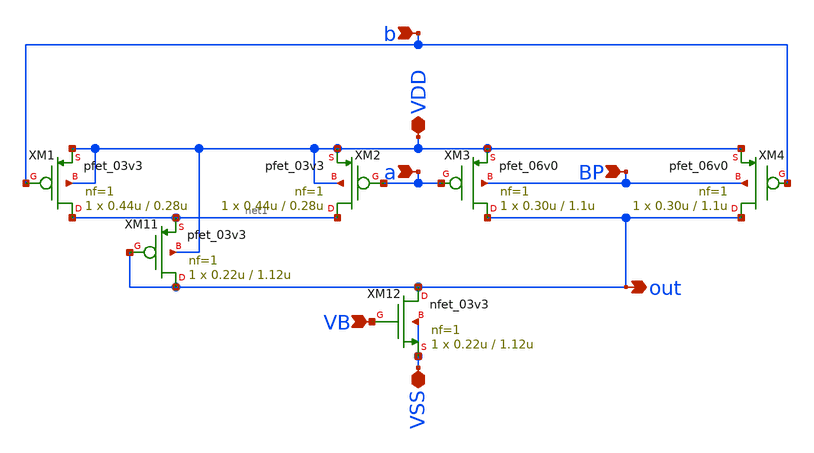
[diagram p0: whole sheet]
** sch_path: xschem_sn2/NMIN.sch
**.subckt NMIN BP VDD out a b VSS VB
*.ipin BP
*.iopin VDD
*.opin out
*.ipin a
*.ipin b
*.iopin VSS
*.ipin VB
XM1 net1 b VDD VDD pfet_03v3 L=0.28u W=0.44u nf=1 ad='int((nf+1)/2) * W/nf * 0.18u' as='int((nf+2)/2) * W/nf * 0.18u'
+ pd='2*int((nf+1)/2) * (W/nf + 0.18u)' ps='2*int((nf+2)/2) * (W/nf + 0.18u)' nrd='0.18u / W' nrs='0.18u / W'
+ sa=0 sb=0 sd=0 m=1 par=1
XM2 net1 a VDD VDD pfet_03v3 L=0.28u W=0.44u nf=1 ad='int((nf+1)/2) * W/nf * 0.18u' as='int((nf+2)/2) * W/nf * 0.18u'
+ pd='2*int((nf+1)/2) * (W/nf + 0.18u)' ps='2*int((nf+2)/2) * (W/nf + 0.18u)' nrd='0.18u / W' nrs='0.18u / W'
+ sa=0 sb=0 sd=0 m=1 par=1
XM3 out a VDD BP pfet_06v0 L=1.1u W=0.30u nf=1 ad='int((nf+1)/2) * W/nf * 0.18u' as='int((nf+2)/2) * W/nf * 0.18u'
+ pd='2*int((nf+1)/2) * (W/nf + 0.18u)' ps='2*int((nf+2)/2) * (W/nf + 0.18u)' nrd='0.18u / W' nrs='0.18u / W'
+ sa=0 sb=0 sd=0 m=1
XM4 out b VDD BP pfet_06v0 L=1.1u W=0.30u nf=1 ad='int((nf+1)/2) * W/nf * 0.18u' as='int((nf+2)/2) * W/nf * 0.18u'
+ pd='2*int((nf+1)/2) * (W/nf + 0.18u)' ps='2*int((nf+2)/2) * (W/nf + 0.18u)' nrd='0.18u / W' nrs='0.18u / W'
+ sa=0 sb=0 sd=0 m=1
XM11 out out net1 VDD pfet_03v3 L=1.12u W=0.22u nf=1 ad='int((nf+1)/2) * W/nf * 0.18u' as='int((nf+2)/2) * W/nf * 0.18u'
+ pd='2*int((nf+1)/2) * (W/nf + 0.18u)' ps='2*int((nf+2)/2) * (W/nf + 0.18u)' nrd='0.18u / W' nrs='0.18u / W'
+ sa=0 sb=0 sd=0 m=1 par=1
XM12 out VB VSS VSS nfet_03v3 L=1.12u W=0.22u nf=1 ad='int((nf+1)/2) * W/nf * 0.18u' as='int((nf+2)/2) * W/nf * 0.18u'
+ pd='2*int((nf+1)/2) * (W/nf + 0.18u)' ps='2*int((nf+2)/2) * (W/nf + 0.18u)' nrd='0.18u / W' nrs='0.18u / W'
+ sa=0 sb=0 sd=0 m=1 par=1
**.ends
.end
